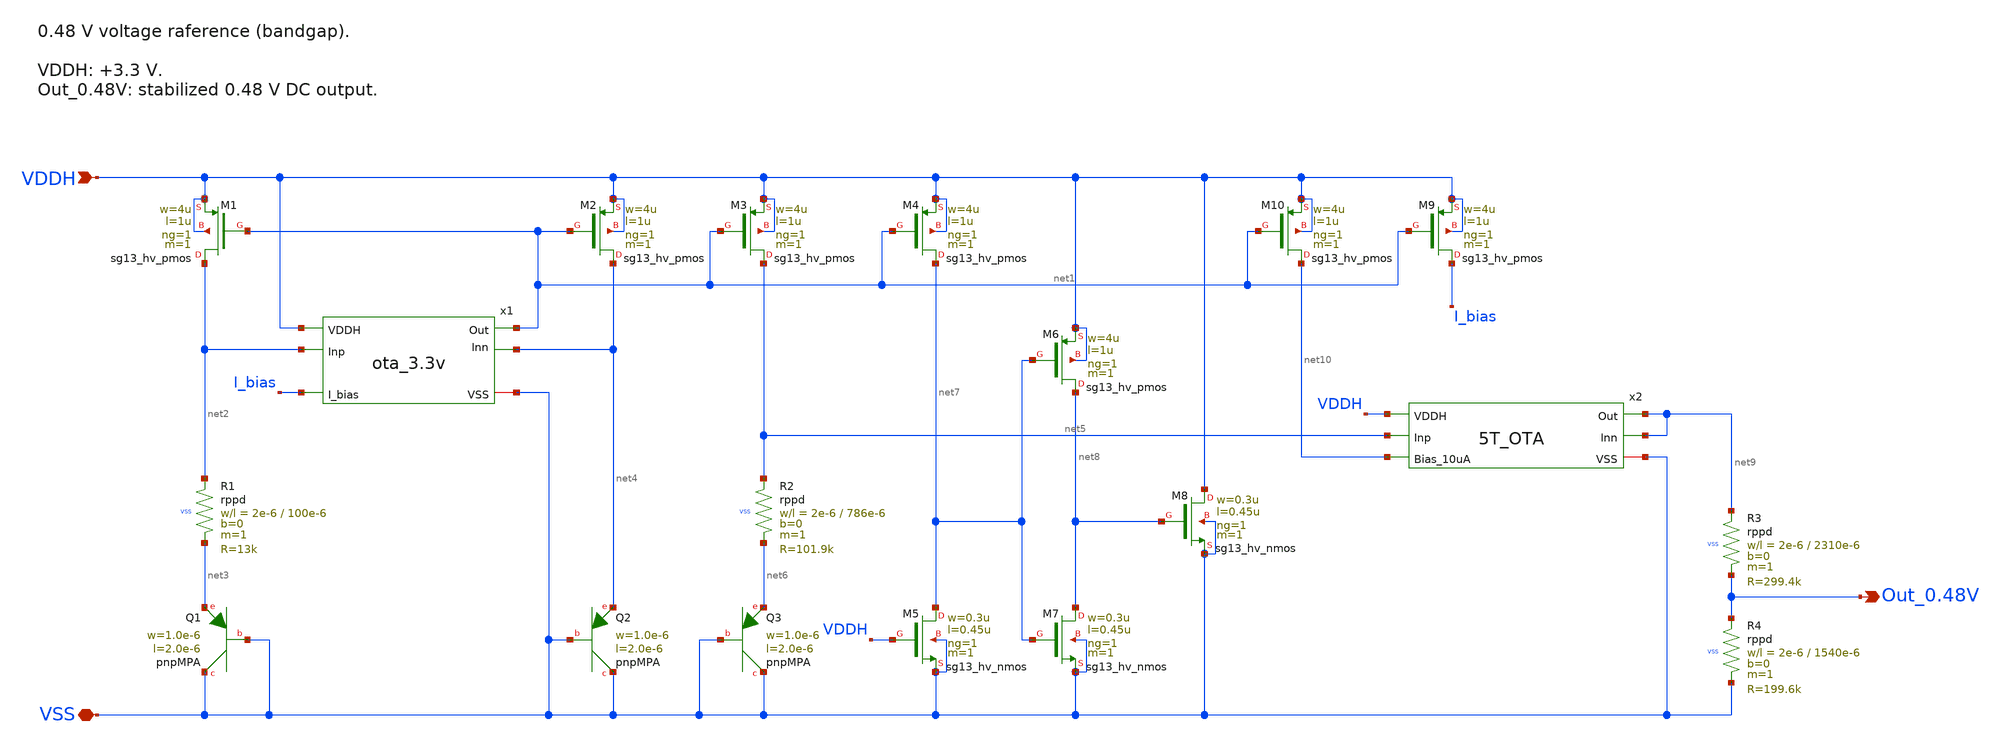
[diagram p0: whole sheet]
** sch_path: sar_adc/xschem/blocks/bandgap/0.48v_bandgap.sch
**.subckt 0.48v_bandgap VDDH VSS Out_0.48V
*.ipin VDDH
*.iopin VSS
*.opin Out_0.48V
XM1 net2 net1 VDDH VDDH sg13_hv_pmos w=4u l=1u ng=1 m=1 mm_ok=1
x1 VDDH net2 net4 net1 I_bias VSS ota_3.3v
XM2 net4 net1 VDDH VDDH sg13_hv_pmos w=4u l=1u ng=1 m=1 mm_ok=1
XR1 net2 net3 VSS rppd w=2e-6 l=100e-6 m=1 b=0 mm_ok=1
XQ1 VSS VSS net3 pnpMPA a=2p p=6u m=8
XQ2 VSS VSS net4 pnpMPA a=2p p=6u m=1
XM3 net5 net1 VDDH VDDH sg13_hv_pmos w=4u l=1u ng=1 m=1 mm_ok=1
XQ3 VSS VSS net6 pnpMPA a=2p p=6u m=1
XR2 net5 net6 VSS rppd w=2e-6 l=786e-6 m=1 b=0 mm_ok=1
XM4 net7 net1 VDDH VDDH sg13_hv_pmos w=4u l=1u ng=1 m=1 mm_ok=1
XM5 net7 VDDH VSS VSS sg13_hv_nmos w=0.3u l=0.45u ng=1 m=1 mm_ok=1
XM6 net8 net7 VDDH VDDH sg13_hv_pmos w=4u l=1u ng=1 m=1 mm_ok=1
XM7 net8 net7 VSS VSS sg13_hv_nmos w=0.3u l=0.45u ng=1 m=1 mm_ok=1
XM8 VDDH net8 VSS VSS sg13_hv_nmos w=0.3u l=0.45u ng=1 m=1 mm_ok=1
XM9 I_bias net1 VDDH VDDH sg13_hv_pmos w=4u l=1u ng=1 m=1 mm_ok=1
x2 VDDH net9 net9 net5 net10 VSS 5T_OTA
XR3 net9 Out_0.48V VSS rppd w=2e-6 l=2310e-6 m=1 b=0 mm_ok=1
XR4 Out_0.48V VSS VSS rppd w=2e-6 l=1540e-6 m=1 b=0 mm_ok=1
XM10 net10 net1 VDDH VDDH sg13_hv_pmos w=4u l=1u ng=1 m=1 mm_ok=1
**.ends

* expanding   symbol:  Projektai/SG13G2/SAR_ADC/ota_3.3v.sym # of pins=6
** sym_path: sar_adc/xschem/blocks/cascode_ota/ota_3.3v.sym
** sch_path: sar_adc/xschem/blocks/cascode_ota/ota_3.3v.sch
.subckt ota_3.3v VDDH Inp Inn Out I_bias VSS
*.ipin VDDH
*.iopin VSS
*.ipin I_bias
*.opin Out
*.ipin Inp
*.ipin Inn
XM2 net1 net1 VDDH VDDH sg13_hv_pmos w=10u l=1u ng=1 m=1 mm_ok=1
XM3 net1 I_bias VSS VSS sg13_hv_nmos w=3u l=3u ng=1 m=1 mm_ok=1
XM1 I_bias I_bias VSS VSS sg13_hv_nmos w=3u l=3u ng=1 m=1 mm_ok=1
XM11 net8 I_bias VSS VSS sg13_hv_nmos w=3u l=3u ng=1 m=1 mm_ok=1
XM13 net5 Inp net2 VDDH sg13_hv_pmos w=8u l=1u ng=2 m=1 mm_ok=1
XM14 net6 Inn net2 VDDH sg13_hv_pmos w=8u l=1u ng=2 m=1 mm_ok=1
XM15 net7 net4 VDDH VDDH sg13_hv_pmos w=10u l=1u ng=1 m=1 mm_ok=1
XM20 net3 net4 VDDH VDDH sg13_hv_pmos w=10u l=1u ng=1 m=1 mm_ok=1
XM17 net4 v_net3 net7 VDDH sg13_hv_pmos w=10u l=1u ng=1 m=1 mm_ok=1
XM18 net4 v_net2 net5 VSS sg13_hv_nmos w=10u l=1u ng=1 m=1 mm_ok=1
XM19 net5 v_net1 VSS VSS sg13_hv_nmos w=9u l=1u ng=1 m=1 mm_ok=1
XM22 Out v_net2 net6 VSS sg13_hv_nmos w=10u l=1u ng=1 m=1 mm_ok=1
XM23 net6 v_net1 VSS VSS sg13_hv_nmos w=9u l=1u ng=1 m=1 mm_ok=1
XM12 net2 net8 VDDH VDDH sg13_hv_pmos w=10u l=1u ng=1 m=1 mm_ok=1
XM10 net8 net8 VDDH VDDH sg13_hv_pmos w=10u l=1u ng=1 m=1 mm_ok=1
XM6 v_net1 v_net1 VSS VSS sg13_hv_nmos w=8u l=1u ng=1 m=1 mm_ok=1
XM4 v_net2 net1 VDDH VDDH sg13_hv_pmos w=10u l=1u ng=1 m=1 mm_ok=1
XM5 v_net2 v_net2 v_net1 VSS sg13_hv_nmos w=10u l=1u ng=2 m=1 mm_ok=1
XM7 net9 net9 VDDH VDDH sg13_hv_pmos w=10u l=1u ng=1 m=1 mm_ok=1
XM9 v_net3 I_bias VSS VSS sg13_hv_nmos w=1.9u l=3u ng=1 m=1 mm_ok=1
XM8 v_net3 v_net3 net9 VDDH sg13_hv_pmos w=10u l=1u ng=1 m=1 mm_ok=1
XM21 Out v_net3 net3 VDDH sg13_hv_pmos w=10u l=1u ng=1 m=1 mm_ok=1
.ends


* expanding   symbol:  Projektai/SG13G2/SAR_ADC/5T_OTA.sym # of pins=6
** sym_path: sar_adc/xschem/blocks/5t_ota/5T_OTA.sym
** sch_path: sar_adc/xschem/blocks/5t_ota/5T_OTA.sch
.subckt 5T_OTA VDDH Out Inn Inp Bias_10uA VSS
*.ipin VDDH
*.opin Out
*.iopin VSS
*.ipin Bias_10uA
*.ipin Inp
*.ipin Inn
XM1 net1 net1 VDDH VDDH sg13_hv_pmos w=5u l=6u ng=1 m=4 mm_ok=1
XM2 Out net1 VDDH VDDH sg13_hv_pmos w=5u l=6u ng=1 m=4 mm_ok=1
XM3 net1 Inp net2 VSS sg13_hv_nmos w=10u l=2u ng=1 m=4 mm_ok=1
XM4 Out Inn net2 VSS sg13_hv_nmos w=10u l=2u ng=1 m=4 mm_ok=1
XM5 net2 Bias_10uA VSS VSS sg13_hv_nmos w=5u l=2u ng=1 m=12 mm_ok=1
XM6 Bias_10uA Bias_10uA VSS VSS sg13_hv_nmos w=5u l=2u ng=1 m=2 mm_ok=1
.ends

.end
